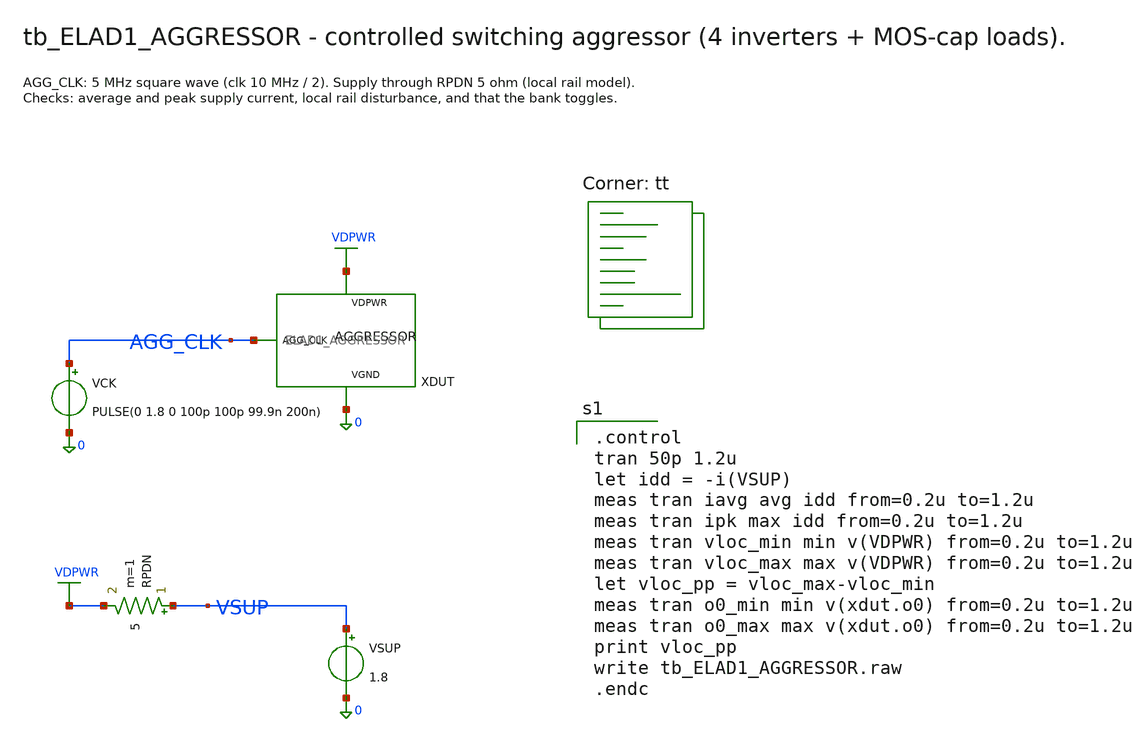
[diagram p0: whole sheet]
** sch_path: cells/ELAD1_AGGRESSOR/schematic/tb_ELAD1_AGGRESSOR.sch
**.subckt tb_ELAD1_AGGRESSOR
XDUT AGG_CLK VDPWR 0 ELAD1_AGGRESSOR
VCK AGG_CLK 0 PULSE(0 1.8 0 100p 100p 99.9n 200n)
RPDN VSUP VDPWR 5 m=1
VSUP VSUP 0 1.8
**** begin user architecture code

.control
tran 50p 1.2u
let idd = -i(VSUP)
meas tran iavg avg idd from=0.2u to=1.2u
meas tran ipk max idd from=0.2u to=1.2u
meas tran vloc_min min v(VDPWR) from=0.2u to=1.2u
meas tran vloc_max max v(VDPWR) from=0.2u to=1.2u
let vloc_pp = vloc_max-vloc_min
meas tran o0_min min v(xdut.o0) from=0.2u to=1.2u
meas tran o0_max max v(xdut.o0) from=0.2u to=1.2u
print vloc_pp
write tb_ELAD1_AGGRESSOR.raw
.endc

.lib $::SKYWATER_MODELS/sky130.lib.spice tt
**** end user architecture code
**.ends

* expanding   symbol:  ELAD1_AGGRESSOR.sym # of pins=3
** sym_path: cells/ELAD1_AGGRESSOR/schematic/ELAD1_AGGRESSOR.sym
** sch_path: cells/ELAD1_AGGRESSOR/schematic/ELAD1_AGGRESSOR.sch
.subckt ELAD1_AGGRESSOR AGG_CLK VDPWR VGND
*.iopin AGG_CLK
*.iopin VDPWR
*.iopin VGND
XB1P b1 AGG_CLK VDPWR VDPWR sky130_fd_pr__pfet_01v8 L=0.15 W=1 nf=1 ad='int((nf+1)/2) * W/nf * 0.29'
+ as='int((nf+2)/2) * W/nf * 0.29' pd='2*int((nf+1)/2) * (W/nf + 0.29)' ps='2*int((nf+2)/2) * (W/nf + 0.29)'
+ nrd='0.29 / W' nrs='0.29 / W' sa=0 sb=0 sd=0 mult=1 m=1
XB1N b1 AGG_CLK VGND VGND sky130_fd_pr__nfet_01v8 L=0.15 W=0.65 nf=1 ad='int((1 + 1)/2) * 0.65 / 1 * 0.29'
+ as='int((1 + 2)/2) * 0.65 / 1 * 0.29' pd='2*int((1 + 1)/2) * (0.65 / 1 + 0.29)' ps='2*int((1 + 2)/2) * (0.65 / 1 + 0.29)'
+ nrd='0.29 / 0.65 ' nrs='0.29 / 0.65 ' sa=0 sb=0 sd=0 mult=1 m=1
XB2P b2 b1 VDPWR VDPWR sky130_fd_pr__pfet_01v8 L=0.15 W=4 nf=1 ad='int((nf+1)/2) * W/nf * 0.29' as='int((nf+2)/2) * W/nf * 0.29'
+ pd='2*int((nf+1)/2) * (W/nf + 0.29)' ps='2*int((nf+2)/2) * (W/nf + 0.29)' nrd='0.29 / W' nrs='0.29 / W'
+ sa=0 sb=0 sd=0 mult=1 m=1
XB2N b2 b1 VGND VGND sky130_fd_pr__nfet_01v8 L=0.15 W=2 nf=1 ad='int((1 + 1)/2) * 2 / 1 * 0.29' as='int((1 + 2)/2) * 2 / 1 * 0.29'
+ pd='2*int((1 + 1)/2) * (2 / 1 + 0.29)' ps='2*int((1 + 2)/2) * (2 / 1 + 0.29)' nrd='0.29 / 2 ' nrs='0.29 / 2 '
+ sa=0 sb=0 sd=0 mult=1 m=1
XIP[3] o3 b2 VDPWR VDPWR sky130_fd_pr__pfet_01v8 L=0.15 W=4 nf=1 ad='int((nf+1)/2) * W/nf * 0.29' as='int((nf+2)/2) * W/nf * 0.29'
+ pd='2*int((nf+1)/2) * (W/nf + 0.29)' ps='2*int((nf+2)/2) * (W/nf + 0.29)' nrd='0.29 / W' nrs='0.29 / W'
+ sa=0 sb=0 sd=0 mult=1 m=1
XIP[2] o2 b2 VDPWR VDPWR sky130_fd_pr__pfet_01v8 L=0.15 W=4 nf=1 ad='int((nf+1)/2) * W/nf * 0.29' as='int((nf+2)/2) * W/nf * 0.29'
+ pd='2*int((nf+1)/2) * (W/nf + 0.29)' ps='2*int((nf+2)/2) * (W/nf + 0.29)' nrd='0.29 / W' nrs='0.29 / W'
+ sa=0 sb=0 sd=0 mult=1 m=1
XIP[1] o1 b2 VDPWR VDPWR sky130_fd_pr__pfet_01v8 L=0.15 W=4 nf=1 ad='int((nf+1)/2) * W/nf * 0.29' as='int((nf+2)/2) * W/nf * 0.29'
+ pd='2*int((nf+1)/2) * (W/nf + 0.29)' ps='2*int((nf+2)/2) * (W/nf + 0.29)' nrd='0.29 / W' nrs='0.29 / W'
+ sa=0 sb=0 sd=0 mult=1 m=1
XIP[0] o0 b2 VDPWR VDPWR sky130_fd_pr__pfet_01v8 L=0.15 W=4 nf=1 ad='int((nf+1)/2) * W/nf * 0.29' as='int((nf+2)/2) * W/nf * 0.29'
+ pd='2*int((nf+1)/2) * (W/nf + 0.29)' ps='2*int((nf+2)/2) * (W/nf + 0.29)' nrd='0.29 / W' nrs='0.29 / W'
+ sa=0 sb=0 sd=0 mult=1 m=1
XIN[3] o3 b2 VGND VGND sky130_fd_pr__nfet_01v8 L=0.15 W=2 nf=1 ad='int((1 + 1)/2) * 2 / 1 * 0.29' as='int((1 + 2)/2) * 2 / 1 * 0.29'
+ pd='2*int((1 + 1)/2) * (2 / 1 + 0.29)' ps='2*int((1 + 2)/2) * (2 / 1 + 0.29)' nrd='0.29 / 2 ' nrs='0.29 / 2 '
+ sa=0 sb=0 sd=0 mult=1 m=1
XIN[2] o2 b2 VGND VGND sky130_fd_pr__nfet_01v8 L=0.15 W=2 nf=1 ad='int((1 + 1)/2) * 2 / 1 * 0.29' as='int((1 + 2)/2) * 2 / 1 * 0.29'
+ pd='2*int((1 + 1)/2) * (2 / 1 + 0.29)' ps='2*int((1 + 2)/2) * (2 / 1 + 0.29)' nrd='0.29 / 2 ' nrs='0.29 / 2 '
+ sa=0 sb=0 sd=0 mult=1 m=1
XIN[1] o1 b2 VGND VGND sky130_fd_pr__nfet_01v8 L=0.15 W=2 nf=1 ad='int((1 + 1)/2) * 2 / 1 * 0.29' as='int((1 + 2)/2) * 2 / 1 * 0.29'
+ pd='2*int((1 + 1)/2) * (2 / 1 + 0.29)' ps='2*int((1 + 2)/2) * (2 / 1 + 0.29)' nrd='0.29 / 2 ' nrs='0.29 / 2 '
+ sa=0 sb=0 sd=0 mult=1 m=1
XIN[0] o0 b2 VGND VGND sky130_fd_pr__nfet_01v8 L=0.15 W=2 nf=1 ad='int((1 + 1)/2) * 2 / 1 * 0.29' as='int((1 + 2)/2) * 2 / 1 * 0.29'
+ pd='2*int((1 + 1)/2) * (2 / 1 + 0.29)' ps='2*int((1 + 2)/2) * (2 / 1 + 0.29)' nrd='0.29 / 2 ' nrs='0.29 / 2 '
+ sa=0 sb=0 sd=0 mult=1 m=1
XC[3] VGND o3 VGND VGND sky130_fd_pr__nfet_01v8 L=4 W=5 nf=1 ad='int((1 + 1)/2) * 5 / 1 * 0.29' as='int((1 + 2)/2) * 5 / 1 * 0.29'
+ pd='2*int((1 + 1)/2) * (5 / 1 + 0.29)' ps='2*int((1 + 2)/2) * (5 / 1 + 0.29)' nrd='0.29 / 5 ' nrs='0.29 / 5 '
+ sa=0 sb=0 sd=0 mult=1 m=1
XC[2] VGND o2 VGND VGND sky130_fd_pr__nfet_01v8 L=4 W=5 nf=1 ad='int((1 + 1)/2) * 5 / 1 * 0.29' as='int((1 + 2)/2) * 5 / 1 * 0.29'
+ pd='2*int((1 + 1)/2) * (5 / 1 + 0.29)' ps='2*int((1 + 2)/2) * (5 / 1 + 0.29)' nrd='0.29 / 5 ' nrs='0.29 / 5 '
+ sa=0 sb=0 sd=0 mult=1 m=1
XC[1] VGND o1 VGND VGND sky130_fd_pr__nfet_01v8 L=4 W=5 nf=1 ad='int((1 + 1)/2) * 5 / 1 * 0.29' as='int((1 + 2)/2) * 5 / 1 * 0.29'
+ pd='2*int((1 + 1)/2) * (5 / 1 + 0.29)' ps='2*int((1 + 2)/2) * (5 / 1 + 0.29)' nrd='0.29 / 5 ' nrs='0.29 / 5 '
+ sa=0 sb=0 sd=0 mult=1 m=1
XC[0] VGND o0 VGND VGND sky130_fd_pr__nfet_01v8 L=4 W=5 nf=1 ad='int((1 + 1)/2) * 5 / 1 * 0.29' as='int((1 + 2)/2) * 5 / 1 * 0.29'
+ pd='2*int((1 + 1)/2) * (5 / 1 + 0.29)' ps='2*int((1 + 2)/2) * (5 / 1 + 0.29)' nrd='0.29 / 5 ' nrs='0.29 / 5 '
+ sa=0 sb=0 sd=0 mult=1 m=1
.ends

.end
